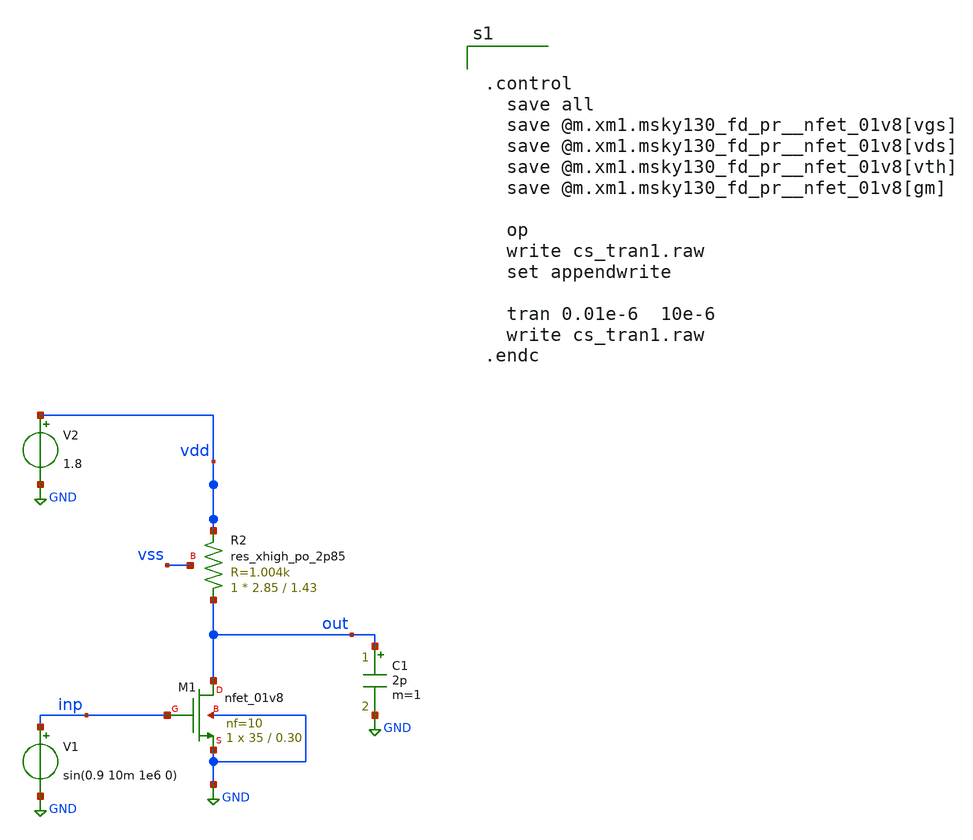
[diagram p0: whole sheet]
** sch_path: xschem/cs_tran1.sch
**.subckt cs_tran1
V1 inp GND sin(0.9 10m 1e6 0)
V2 vdd GND 1.8
C1 out GND 2p m=1
XM1 out inp GND GND sky130_fd_pr__nfet_01v8 L=0.30 W=35 nf=10 ad='int((nf+1)/2) * W/nf * 0.29' as='int((nf+2)/2) * W/nf * 0.29'
+ pd='2*int((nf+1)/2) * (W/nf + 0.29)' ps='2*int((nf+2)/2) * (W/nf + 0.29)' nrd='0.29 / W' nrs='0.29 / W'
+ sa=0 sb=0 sd=0 mult=1 m=1
XR2 out vdd vss sky130_fd_pr__res_xhigh_po_2p85 L=1.43 mult=1 m=1
**** begin user architecture code

** opencircuitdesign pdks install
.lib $::SKYWATER_MODELS/sky130.lib.spice tt




.control
  save all
  save @m.xm1.msky130_fd_pr__nfet_01v8[vgs]
  save @m.xm1.msky130_fd_pr__nfet_01v8[vds]
  save @m.xm1.msky130_fd_pr__nfet_01v8[vth]
  save @m.xm1.msky130_fd_pr__nfet_01v8[gm]

  op
  write cs_tran1.raw
  set appendwrite

  tran 0.01e-6  10e-6
  write cs_tran1.raw
.endc


**** end user architecture code
**.ends
.GLOBAL GND
.end
